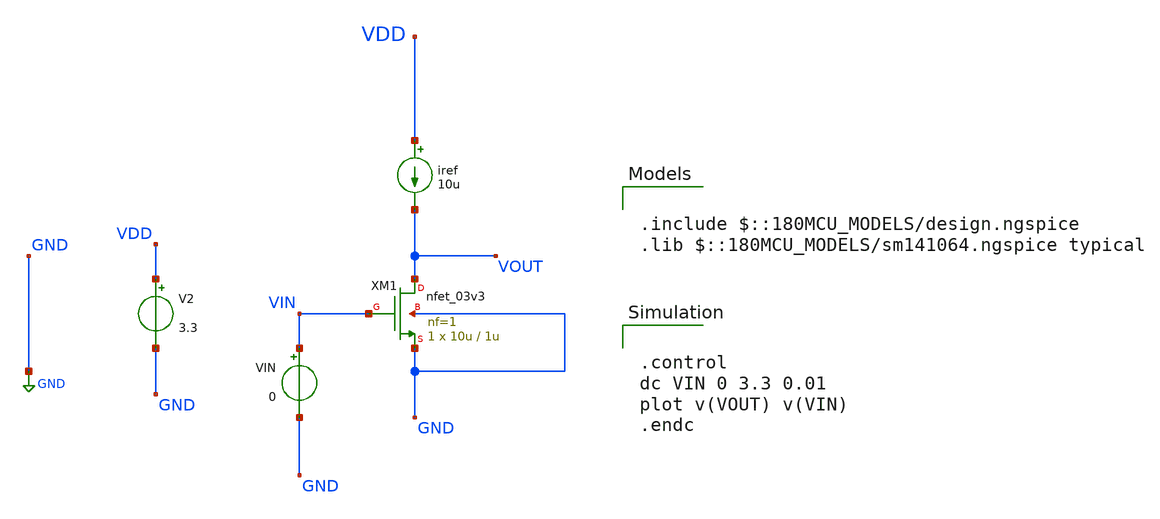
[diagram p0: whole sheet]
** sch_path: designs/libs/session_2/cs_active_load_dc_bias.sch
**.subckt cs_active_load_dc_bias
XM1 VOUT VIN GND GND nfet_03v3 L=1u W=10u nf=1 ad='int((nf+1)/2) * W/nf * 0.18u' as='int((nf+2)/2) * W/nf * 0.18u'
+ pd='2*int((nf+1)/2) * (W/nf + 0.18u)' ps='2*int((nf+2)/2) * (W/nf + 0.18u)' nrd='0.18u / W' nrs='0.18u / W'
+ sa=0 sb=0 sd=0 m=1
V2 VDD GND 3.3
VIN VIN GND 0
iref VDD VOUT 10u
**** begin user architecture code


.control
dc VIN 0 3.3 0.01
plot v(VOUT) v(VIN)
.endc



.include $::180MCU_MODELS/design.ngspice
.lib $::180MCU_MODELS/sm141064.ngspice typical

**** end user architecture code
**.ends
.GLOBAL GND
.end
